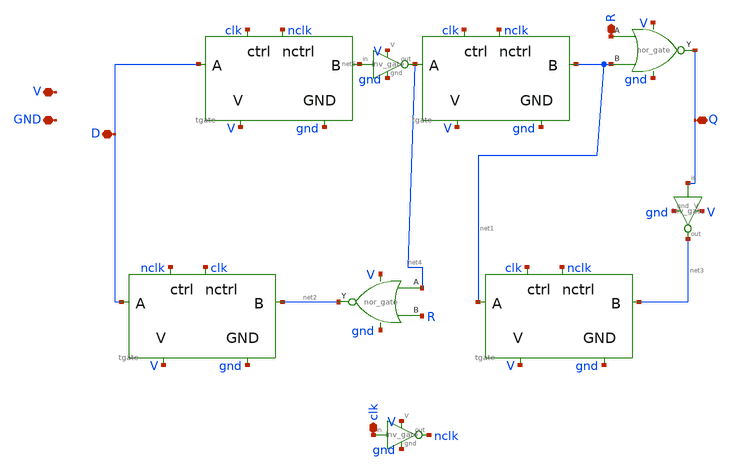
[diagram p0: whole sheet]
** sch_path: SAR_ADC/xschem/designs/ffdr.sch
* SAR_ADC/xschem/designs/inv_gate.sym:
* Copyright 2022 Stefan Frederik Schippers
* Licensed under the Apache License, Version 2.0 (the "License");
**.subckt ffdr R clk Q D V GND
*.iopin R
*.iopin clk
*.iopin Q
*.iopin D
*.iopin V
*.iopin GND
X2 D V gnd net5 nclk clk tgate
X3 Q net1 R V gnd nor_gate
X1 V gnd net5 net4 inv_gate
X4 net4 V gnd net1 nclk clk tgate
X5 D V gnd net2 clk nclk tgate
X6 net1 V gnd net3 nclk clk tgate
X7 V gnd clk nclk inv_gate
X8 net2 R net4 V gnd nor_gate
X9 V gnd Q net3 inv_gate
**.ends

* expanding   symbol:  tgate.sym # of pins=6
** sym_path: SAR_ADC/xschem/designs/tgate.sym
** sch_path: SAR_ADC/xschem/designs/tgate.sch
.subckt tgate A V GND B nctrl ctrl
*.iopin ctrl
*.iopin A
*.iopin B
*.iopin nctrl
*.iopin GND
*.iopin V
XM1 A ctrl B GND sky130_fd_pr__nfet_01v8 L=0.15 W=1 nf=1 ad='int((nf+1)/2) * W/nf * 0.29' as='int((nf+2)/2) * W/nf * 0.29'
+ pd='2*int((nf+1)/2) * (W/nf + 0.29)' ps='2*int((nf+2)/2) * (W/nf + 0.29)' nrd='0.29 / W' nrs='0.29 / W'
+ sa=0 sb=0 sd=0 mult=1 m=1
XM2 B nctrl A V sky130_fd_pr__nfet_01v8 L=0.15 W=1 nf=1 ad='int((nf+1)/2) * W/nf * 0.29' as='int((nf+2)/2) * W/nf * 0.29'
+ pd='2*int((nf+1)/2) * (W/nf + 0.29)' ps='2*int((nf+2)/2) * (W/nf + 0.29)' nrd='0.29 / W' nrs='0.29 / W'
+ sa=0 sb=0 sd=0 mult=1 m=1
.ends


* expanding   symbol:  nor_gate.sym # of pins=5
** sym_path: SAR_ADC/xschem/designs/nor_gate.sym
** sch_path: SAR_ADC/xschem/designs/nor_gate.sch
.subckt nor_gate out B A V gnd
*.iopin A
*.iopin out
*.iopin gnd
*.iopin V
*.iopin B
XM1 gnd A gnd gnd sky130_fd_pr__nfet_01v8 L=0.15 W=1 nf=1 ad='int((nf+1)/2) * W/nf * 0.29' as='int((nf+2)/2) * W/nf * 0.29'
+ pd='2*int((nf+1)/2) * (W/nf + 0.29)' ps='2*int((nf+2)/2) * (W/nf + 0.29)' nrd='0.29 / W' nrs='0.29 / W'
+ sa=0 sb=0 sd=0 mult=1 m=1
XM2 net1 A V V sky130_fd_pr__nfet_01v8 L=0.15 W=1 nf=1 ad='int((nf+1)/2) * W/nf * 0.29' as='int((nf+2)/2) * W/nf * 0.29'
+ pd='2*int((nf+1)/2) * (W/nf + 0.29)' ps='2*int((nf+2)/2) * (W/nf + 0.29)' nrd='0.29 / W' nrs='0.29 / W'
+ sa=0 sb=0 sd=0 mult=1 m=1
XM3 out B gnd gnd sky130_fd_pr__nfet_01v8 L=0.15 W=1 nf=1 ad='int((nf+1)/2) * W/nf * 0.29' as='int((nf+2)/2) * W/nf * 0.29'
+ pd='2*int((nf+1)/2) * (W/nf + 0.29)' ps='2*int((nf+2)/2) * (W/nf + 0.29)' nrd='0.29 / W' nrs='0.29 / W'
+ sa=0 sb=0 sd=0 mult=1 m=1
XM4 out B net1 V sky130_fd_pr__nfet_01v8 L=0.15 W=1 nf=1 ad='int((nf+1)/2) * W/nf * 0.29' as='int((nf+2)/2) * W/nf * 0.29'
+ pd='2*int((nf+1)/2) * (W/nf + 0.29)' ps='2*int((nf+2)/2) * (W/nf + 0.29)' nrd='0.29 / W' nrs='0.29 / W'
+ sa=0 sb=0 sd=0 mult=1 m=1
.ends


* expanding   symbol:  inv_gate.sym # of pins=4
** sym_path: SAR_ADC/xschem/designs/inv_gate.sym
** sch_path: SAR_ADC/xschem/designs/inv_gate.sch
.subckt inv_gate V gnd in out
*.iopin in
*.iopin out
*.iopin gnd
*.iopin V
XM1 out in gnd gnd sky130_fd_pr__nfet_01v8 L=0.15 W=1 nf=1 ad='int((nf+1)/2) * W/nf * 0.29' as='int((nf+2)/2) * W/nf * 0.29'
+ pd='2*int((nf+1)/2) * (W/nf + 0.29)' ps='2*int((nf+2)/2) * (W/nf + 0.29)' nrd='0.29 / W' nrs='0.29 / W'
+ sa=0 sb=0 sd=0 mult=1 m=1
XM2 out in V V sky130_fd_pr__nfet_01v8 L=0.15 W=1 nf=1 ad='int((nf+1)/2) * W/nf * 0.29' as='int((nf+2)/2) * W/nf * 0.29'
+ pd='2*int((nf+1)/2) * (W/nf + 0.29)' ps='2*int((nf+2)/2) * (W/nf + 0.29)' nrd='0.29 / W' nrs='0.29 / W'
+ sa=0 sb=0 sd=0 mult=1 m=1
.ends

.end
